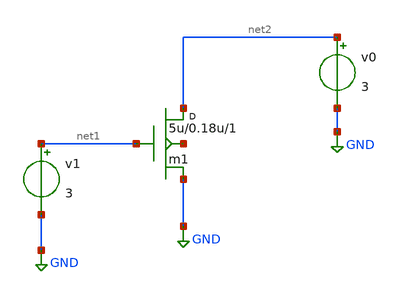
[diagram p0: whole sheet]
** sch_path: schematic/tb_nmos_iv.sch
**.subckt tb_nmos_iv
m1 net2 net1 GND net3 nmos w=5u l=0.18u m=1
v0 net2 GND 3
v1 net1 GND 3
**** begin user architecture code

blabla

**** end user architecture code
**.ends
.GLOBAL GND
.end
